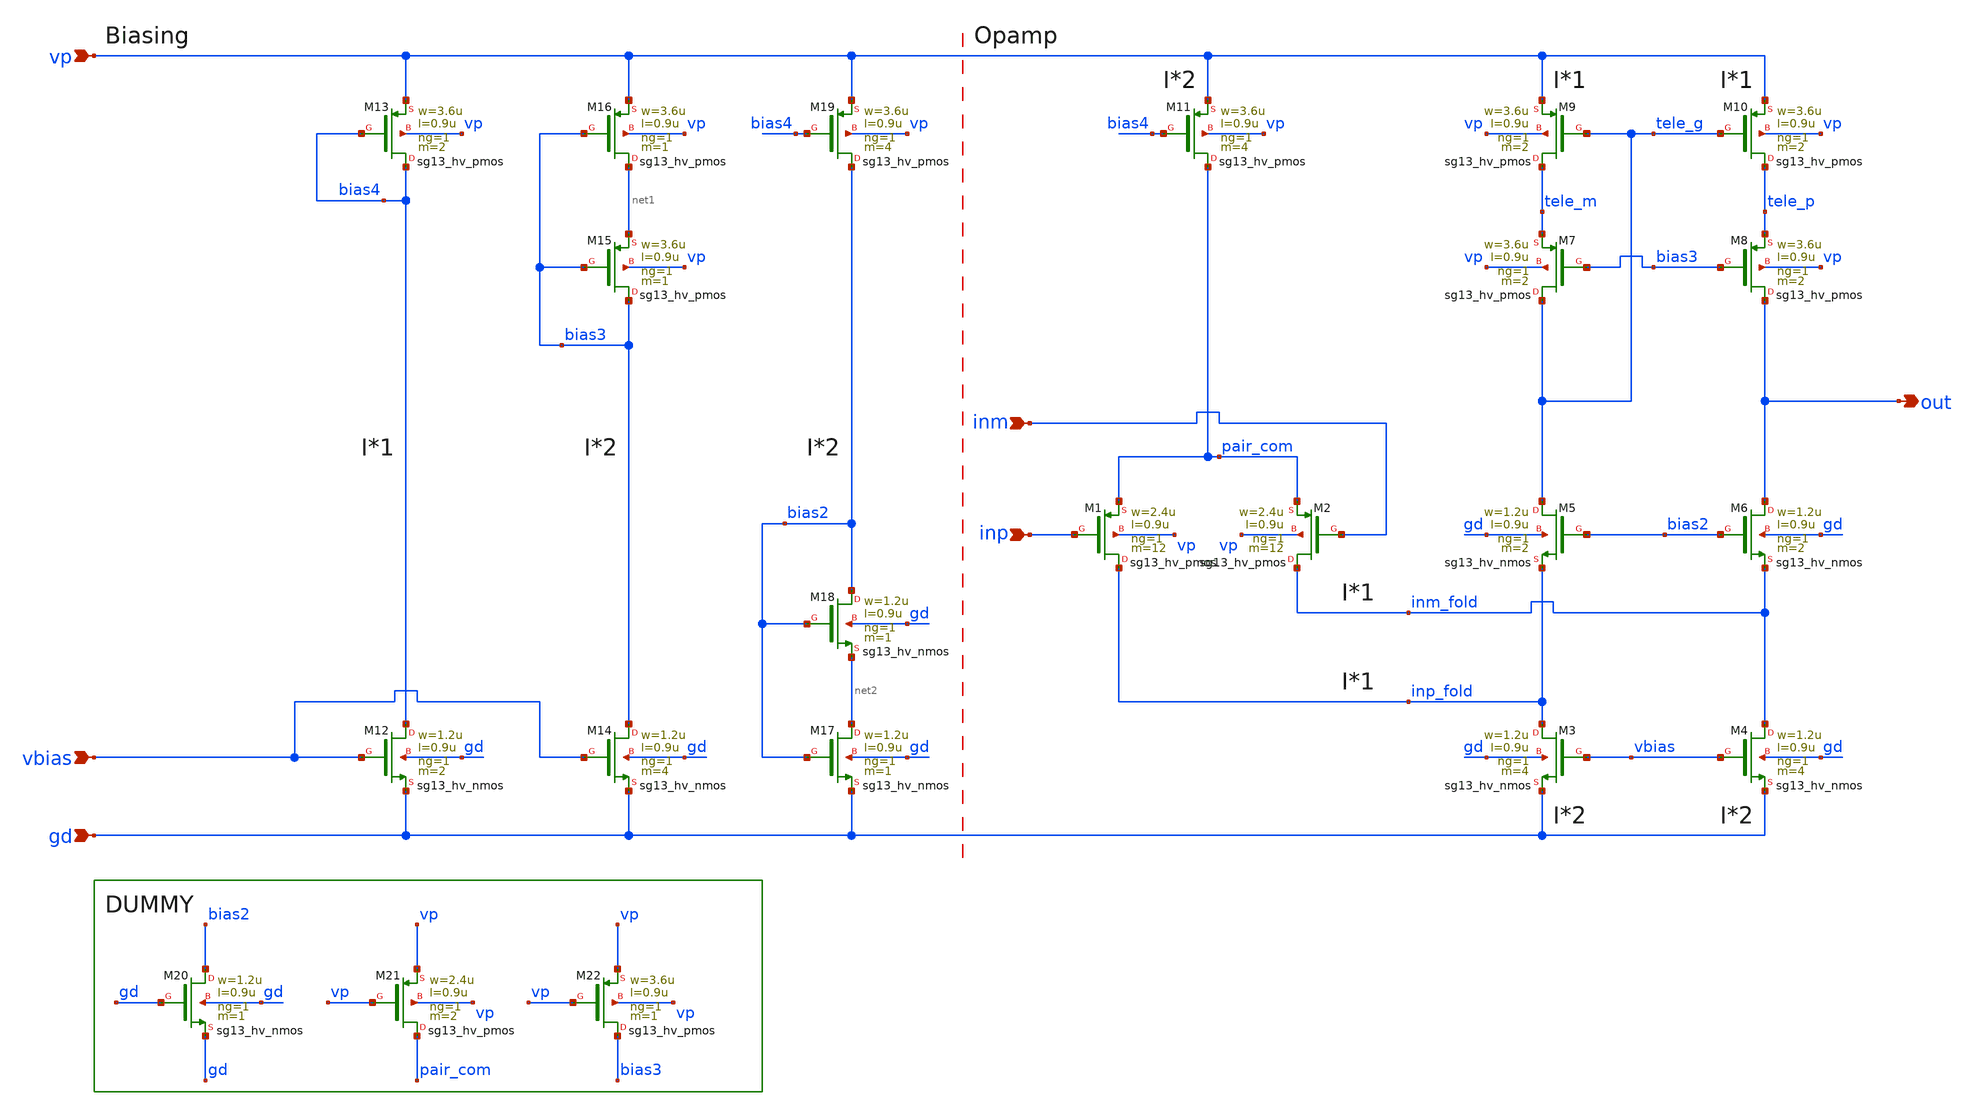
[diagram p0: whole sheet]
** sch_path: circuit/opamp_folded_pmos_buf.sch
**.subckt opamp_folded_pmos_buf vbias inp inm out gd vp
*.ipin vbias
*.ipin inp
*.ipin inm
*.opin out
*.ipin gd
*.ipin vp
XM12 bias4 vbias gd gd sg13_hv_nmos w=1.2u l=0.9u ng=1 m=2 mm_ok=1
XM13 bias4 bias4 vp vp sg13_hv_pmos w=3.6u l=0.9u ng=1 m=2 mm_ok=1
XM11 pair_com bias4 vp vp sg13_hv_pmos w=3.6u l=0.9u ng=1 m=4 mm_ok=1
XM1 inp_fold inp pair_com vp sg13_hv_pmos w=2.4u l=0.9u ng=1 m=12 mm_ok=1
XM2 inm_fold inm pair_com vp sg13_hv_pmos w=2.4u l=0.9u ng=1 m=12 mm_ok=1
XM9 tele_m tele_g vp vp sg13_hv_pmos w=3.6u l=0.9u ng=1 m=2 mm_ok=1
XM10 tele_p tele_g vp vp sg13_hv_pmos w=3.6u l=0.9u ng=1 m=2 mm_ok=1
XM7 tele_g bias3 tele_m vp sg13_hv_pmos w=3.6u l=0.9u ng=1 m=2 mm_ok=1
XM8 out bias3 tele_p vp sg13_hv_pmos w=3.6u l=0.9u ng=1 m=2 mm_ok=1
XM3 inp_fold vbias gd gd sg13_hv_nmos w=1.2u l=0.9u ng=1 m=4 mm_ok=1
XM4 inm_fold vbias gd gd sg13_hv_nmos w=1.2u l=0.9u ng=1 m=4 mm_ok=1
XM5 tele_g bias2 inp_fold gd sg13_hv_nmos w=1.2u l=0.9u ng=1 m=2 mm_ok=1
XM6 out bias2 inm_fold gd sg13_hv_nmos w=1.2u l=0.9u ng=1 m=2 mm_ok=1
XM14 bias3 vbias gd gd sg13_hv_nmos w=1.2u l=0.9u ng=1 m=4 mm_ok=1
XM15 bias3 bias3 net1 vp sg13_hv_pmos w=3.6u l=0.9u ng=1 m=1 mm_ok=1
XM16 net1 bias3 vp vp sg13_hv_pmos w=3.6u l=0.9u ng=1 m=1 mm_ok=1
XM19 bias2 bias4 vp vp sg13_hv_pmos w=3.6u l=0.9u ng=1 m=4 mm_ok=1
XM17 net2 bias2 gd gd sg13_hv_nmos w=1.2u l=0.9u ng=1 m=1 mm_ok=1
XM18 bias2 bias2 net2 gd sg13_hv_nmos w=1.2u l=0.9u ng=1 m=1 mm_ok=1
XM20 bias2 gd gd gd sg13_hv_nmos w=1.2u l=0.9u ng=1 m=1 mm_ok=1
XM21 pair_com vp vp vp sg13_hv_pmos w=2.4u l=0.9u ng=1 m=2 mm_ok=1
XM22 bias3 vp vp vp sg13_hv_pmos w=3.6u l=0.9u ng=1 m=1 mm_ok=1
**.ends
.end
